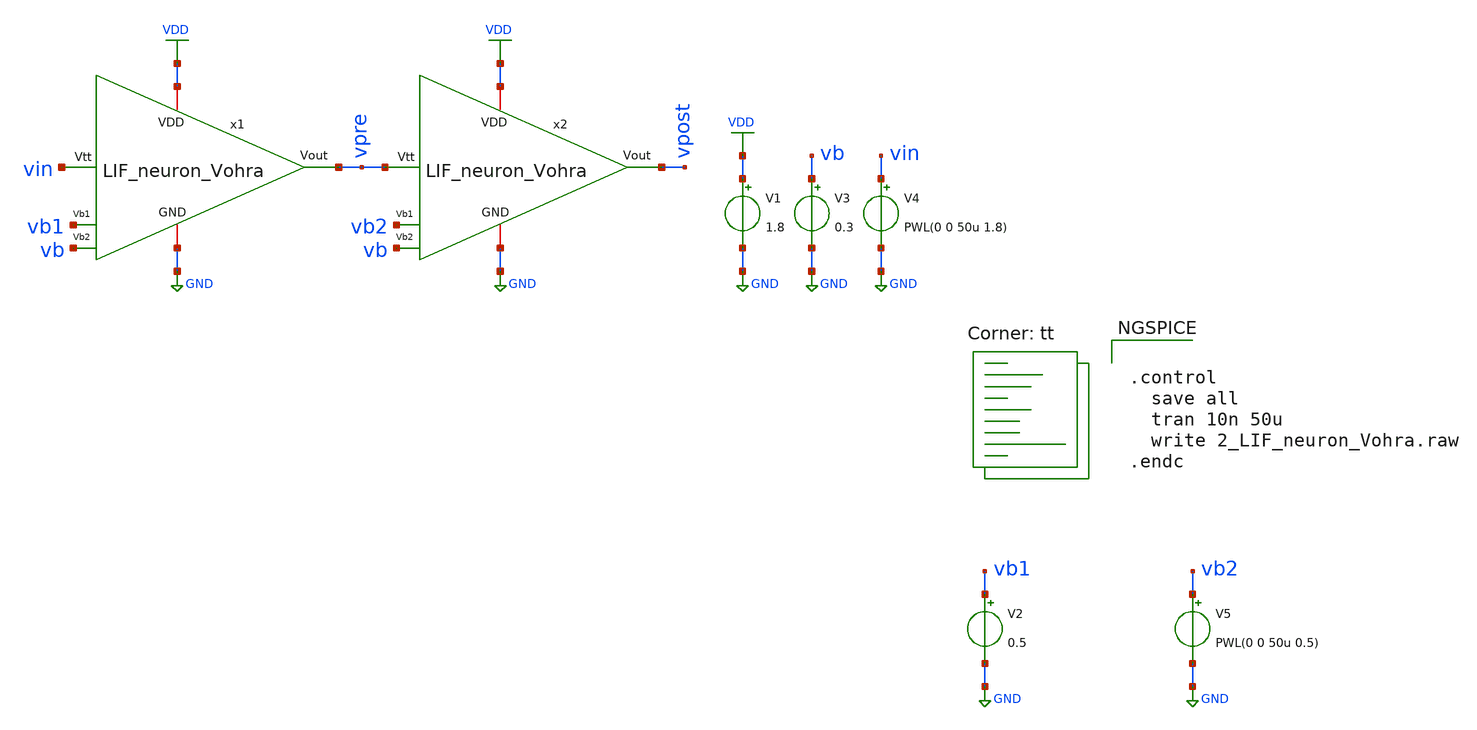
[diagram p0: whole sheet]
** sch_path: LIF_neuron/2_LIF_neuron_Vohra.sch
**.subckt 2_LIF_neuron_Vohra
x1 VDD vpre vb1 vin GND vb LIF_neuron_Vohra
V1 VDD GND 1.8
V4 vin GND PWL(0 0 50u 1.8)
V2 vb1 GND 0.5
V3 vb GND 0.3
x2 VDD vpost vb2 vpre GND vb LIF_neuron_Vohra
V5 vb2 GND PWL(0 0 50u 0.5)
**** begin user architecture code
.lib $::SKYWATER_MODELS/sky130.lib.spice tt


.control
  save all
  tran 10n 50u
  write 2_LIF_neuron_Vohra.raw
.endc


**** end user architecture code
**.ends

* expanding   symbol:  /home/ricardo/RATT_repos/Proyectos_xschem/LIF_neuron/LIF_neuron_Vohra.sym #
*+ of pins=6
** sym_path: LIF_neuron/LIF_neuron_Vohra.sym
** sch_path: LIF_neuron/LIF_neuron_Vohra.sch
.subckt LIF_neuron_Vohra VDD Vout Vb1 Vtt GND Vb2
*.ipin Vtt
*.iopin GND
*.ipin Vb1
*.ipin Vb2
*.iopin VDD
*.opin Vout
XM1 net4 Vtt GND GND sky130_fd_pr__nfet_01v8 L=1 W=0.6 nf=1 ad='int((nf+1)/2) * W/nf * 0.29' as='int((nf+2)/2) * W/nf * 0.29'
+ pd='2*int((nf+1)/2) * (W/nf + 0.29)' ps='2*int((nf+2)/2) * (W/nf + 0.29)' nrd='0.29 / W' nrs='0.29 / W'
+ sa=0 sb=0 sd=0 mult=1 m=1
XM3 net4 net4 VDD VDD sky130_fd_pr__pfet_01v8 L=1 W=0.6 nf=1 ad='int((nf+1)/2) * W/nf * 0.29' as='int((nf+2)/2) * W/nf * 0.29'
+ pd='2*int((nf+1)/2) * (W/nf + 0.29)' ps='2*int((nf+2)/2) * (W/nf + 0.29)' nrd='0.29 / W' nrs='0.29 / W'
+ sa=0 sb=0 sd=0 mult=1 m=1
XM13 net3 Vb1 GND GND sky130_fd_pr__nfet_01v8 L=0.5 W=5 nf=1 ad='int((nf+1)/2) * W/nf * 0.29' as='int((nf+2)/2) * W/nf * 0.29'
+ pd='2*int((nf+1)/2) * (W/nf + 0.29)' ps='2*int((nf+2)/2) * (W/nf + 0.29)' nrd='0.29 / W' nrs='0.29 / W'
+ sa=0 sb=0 sd=0 mult=1 m=1
XM12 net1 net2 net3 GND sky130_fd_pr__nfet_01v8 L=1 W=1 nf=1 ad='int((nf+1)/2) * W/nf * 0.29' as='int((nf+2)/2) * W/nf * 0.29'
+ pd='2*int((nf+1)/2) * (W/nf + 0.29)' ps='2*int((nf+2)/2) * (W/nf + 0.29)' nrd='0.29 / W' nrs='0.29 / W'
+ sa=0 sb=0 sd=0 mult=1 m=1
XM11 net1 net2 VDD VDD sky130_fd_pr__pfet_01v8 L=1 W=1 nf=1 ad='int((nf+1)/2) * W/nf * 0.29' as='int((nf+2)/2) * W/nf * 0.29'
+ pd='2*int((nf+1)/2) * (W/nf + 0.29)' ps='2*int((nf+2)/2) * (W/nf + 0.29)' nrd='0.29 / W' nrs='0.29 / W'
+ sa=0 sb=0 sd=0 mult=1 m=1
XC1 net1 GND sky130_fd_pr__cap_mim_m3_1 W=21 L=1 MF=1 m=1
XM14 net5 net1 GND GND sky130_fd_pr__nfet_01v8 L=1 W=1 nf=1 ad='int((nf+1)/2) * W/nf * 0.29' as='int((nf+2)/2) * W/nf * 0.29'
+ pd='2*int((nf+1)/2) * (W/nf + 0.29)' ps='2*int((nf+2)/2) * (W/nf + 0.29)' nrd='0.29 / W' nrs='0.29 / W'
+ sa=0 sb=0 sd=0 mult=1 m=1
XM4 net5 net4 VDD VDD sky130_fd_pr__pfet_01v8 L=1 W=1 nf=1 ad='int((nf+1)/2) * W/nf * 0.29' as='int((nf+2)/2) * W/nf * 0.29'
+ pd='2*int((nf+1)/2) * (W/nf + 0.29)' ps='2*int((nf+2)/2) * (W/nf + 0.29)' nrd='0.29 / W' nrs='0.29 / W'
+ sa=0 sb=0 sd=0 mult=1 m=1
XC2 net5 GND sky130_fd_pr__cap_mim_m3_1 W=10 L=1 MF=50 m=50
XM5 net5 Vb2 GND GND sky130_fd_pr__nfet_01v8 L=1 W=2 nf=1 ad='int((nf+1)/2) * W/nf * 0.29' as='int((nf+2)/2) * W/nf * 0.29'
+ pd='2*int((nf+1)/2) * (W/nf + 0.29)' ps='2*int((nf+2)/2) * (W/nf + 0.29)' nrd='0.29 / W' nrs='0.29 / W'
+ sa=0 sb=0 sd=0 mult=1 m=1
XM6 net6 Vout GND GND sky130_fd_pr__nfet_01v8 L=1 W=1 nf=1 ad='int((nf+1)/2) * W/nf * 0.29' as='int((nf+2)/2) * W/nf * 0.29'
+ pd='2*int((nf+1)/2) * (W/nf + 0.29)' ps='2*int((nf+2)/2) * (W/nf + 0.29)' nrd='0.29 / W' nrs='0.29 / W'
+ sa=0 sb=0 sd=0 mult=1 m=1
XM7 net2 net5 net6 GND sky130_fd_pr__nfet_01v8 L=1 W=1 nf=1 ad='int((nf+1)/2) * W/nf * 0.29' as='int((nf+2)/2) * W/nf * 0.29'
+ pd='2*int((nf+1)/2) * (W/nf + 0.29)' ps='2*int((nf+2)/2) * (W/nf + 0.29)' nrd='0.29 / W' nrs='0.29 / W'
+ sa=0 sb=0 sd=0 mult=1 m=1
XM8 net2 net5 VDD VDD sky130_fd_pr__pfet_01v8 L=1 W=1 nf=1 ad='int((nf+1)/2) * W/nf * 0.29' as='int((nf+2)/2) * W/nf * 0.29'
+ pd='2*int((nf+1)/2) * (W/nf + 0.29)' ps='2*int((nf+2)/2) * (W/nf + 0.29)' nrd='0.29 / W' nrs='0.29 / W'
+ sa=0 sb=0 sd=0 mult=1 m=1
XM9 Vout net2 net6 GND sky130_fd_pr__nfet_01v8 L=1 W=1 nf=1 ad='int((nf+1)/2) * W/nf * 0.29' as='int((nf+2)/2) * W/nf * 0.29'
+ pd='2*int((nf+1)/2) * (W/nf + 0.29)' ps='2*int((nf+2)/2) * (W/nf + 0.29)' nrd='0.29 / W' nrs='0.29 / W'
+ sa=0 sb=0 sd=0 mult=1 m=1
XM10 Vout net2 VDD VDD sky130_fd_pr__pfet_01v8 L=1 W=5 nf=1 ad='int((nf+1)/2) * W/nf * 0.29' as='int((nf+2)/2) * W/nf * 0.29'
+ pd='2*int((nf+1)/2) * (W/nf + 0.29)' ps='2*int((nf+2)/2) * (W/nf + 0.29)' nrd='0.29 / W' nrs='0.29 / W'
+ sa=0 sb=0 sd=0 mult=1 m=1
.ends

.GLOBAL GND
.GLOBAL VDD
.end
